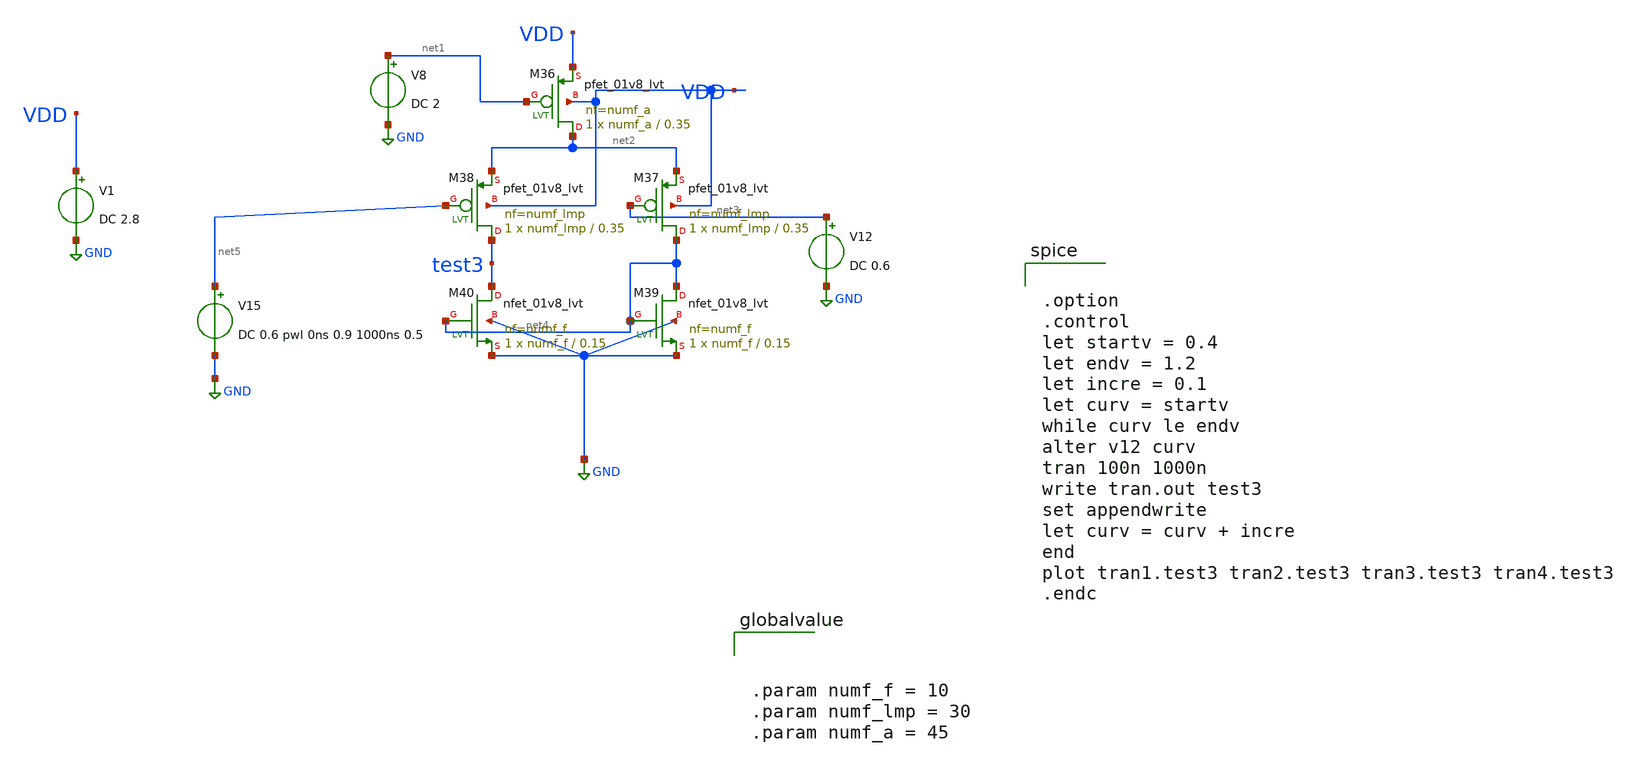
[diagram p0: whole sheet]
** sch_path: level_ctrl.sch
**.subckt level_ctrl
XM36 net2 net1 VDD VDD sky130_fd_pr__pfet_01v8_lvt L=0.35 W=numf_a nf=numf_a ad='int((nf+1)/2) * W/nf * 0.29'
+ as='int((nf+2)/2) * W/nf * 0.29' pd='2*int((nf+1)/2) * (W/nf + 0.29)' ps='2*int((nf+2)/2) * (W/nf + 0.29)'
+ nrd='0.29 / W' nrs='0.29 / W' sa=0 sb=0 sd=0 mult=1 m=1
XM37 net4 net3 net2 VDD sky130_fd_pr__pfet_01v8_lvt L=0.35 W=numf_lmp nf=numf_lmp ad='int((nf+1)/2) * W/nf * 0.29'
+ as='int((nf+2)/2) * W/nf * 0.29' pd='2*int((nf+1)/2) * (W/nf + 0.29)' ps='2*int((nf+2)/2) * (W/nf + 0.29)'
+ nrd='0.29 / W' nrs='0.29 / W' sa=0 sb=0 sd=0 mult=1 m=1
XM38 test3 net5 net2 VDD sky130_fd_pr__pfet_01v8_lvt L=0.35 W=numf_lmp nf=numf_lmp ad='int((nf+1)/2) * W/nf * 0.29'
+ as='int((nf+2)/2) * W/nf * 0.29' pd='2*int((nf+1)/2) * (W/nf + 0.29)' ps='2*int((nf+2)/2) * (W/nf + 0.29)'
+ nrd='0.29 / W' nrs='0.29 / W' sa=0 sb=0 sd=0 mult=1 m=1
V8 net1 GND DC 2
XM39 net4 net4 GND GND sky130_fd_pr__nfet_01v8_lvt L=0.15 W=numf_f nf=numf_f ad='int((nf+1)/2) * W/nf * 0.29'
+ as='int((nf+2)/2) * W/nf * 0.29' pd='2*int((nf+1)/2) * (W/nf + 0.29)' ps='2*int((nf+2)/2) * (W/nf + 0.29)'
+ nrd='0.29 / W' nrs='0.29 / W' sa=0 sb=0 sd=0 mult=1 m=1
XM40 test3 net4 GND GND sky130_fd_pr__nfet_01v8_lvt L=0.15 W=numf_f nf=numf_f ad='int((nf+1)/2) * W/nf * 0.29'
+ as='int((nf+2)/2) * W/nf * 0.29' pd='2*int((nf+1)/2) * (W/nf + 0.29)' ps='2*int((nf+2)/2) * (W/nf + 0.29)'
+ nrd='0.29 / W' nrs='0.29 / W' sa=0 sb=0 sd=0 mult=1 m=1
V12 net3 GND DC 0.6
V15 net5 GND DC 0.6 pwl 0ns 0.9 1000ns 0.5
V1 VDD GND DC 2.8
**** begin user architecture code

** opencircuitdesign pdks install
.lib $::SKYWATER_MODELS/sky130.lib.spice tt_mm




.option
.control
let startv = 0.4
let endv = 1.2
let incre = 0.1
let curv = startv
while curv le endv
alter v12 curv
tran 100n 1000n
write tran.out test3
set appendwrite
let curv = curv + incre
end
plot tran1.test3 tran2.test3 tran3.test3 tran4.test3
.endc





.param numf_f = 10
.param numf_lmp = 30
.param numf_a = 45


**** end user architecture code
**.ends
.GLOBAL GND
.end
